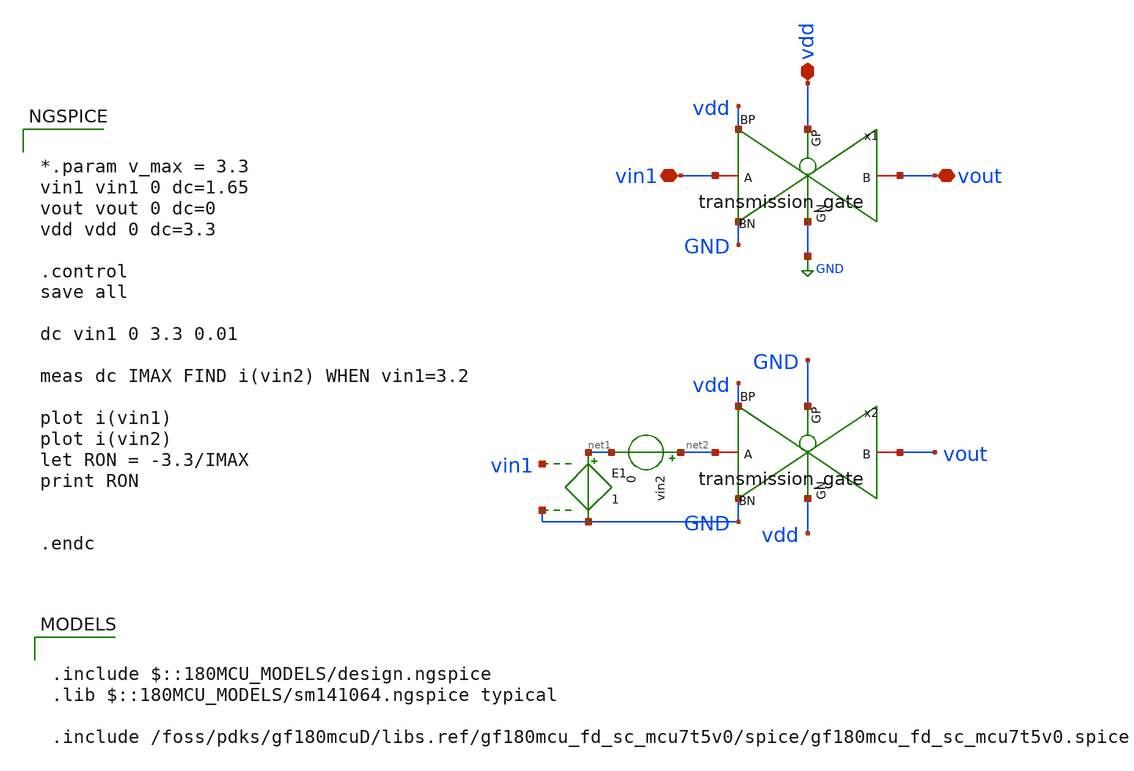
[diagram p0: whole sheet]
** sch_path: designs/switch_matrix_gf180mcu_9t5v0-main/tgate_PK_5V/old/tb_transmission_gate.sch
**.subckt tb_transmission_gate vin1 vout vdd
*.iopin vin1
*.iopin vout
*.iopin vdd
x1 vout GND vdd vin1 vdd GND transmission_gate
x2 vout vdd GND net2 vdd GND transmission_gate
E1 net1 GND vin1 GND 1
vin2 net2 net1 0
**** begin user architecture code


*.param v_max = 3.3
vin1 vin1 0 dc=1.65
vout vout 0 dc=0
vdd vdd 0 dc=3.3

.control
save all

dc vin1 0 3.3 0.01

meas dc IMAX FIND i(vin2) WHEN vin1=3.2

plot i(vin1)
plot i(vin2)
let RON = -3.3/IMAX
print RON


.endc



.include $::180MCU_MODELS/design.ngspice
.lib $::180MCU_MODELS/sm141064.ngspice typical

.include /foss/pdks/gf180mcuD/libs.ref/gf180mcu_fd_sc_mcu7t5v0/spice/gf180mcu_fd_sc_mcu7t5v0.spice

**** end user architecture code
**.ends

* expanding   symbol:  transmission_gate.sym # of pins=6
** sym_path: designs/switch_matrix_gf180mcu_9t5v0-main/tgate_PK/transmission_gate.sym
** sch_path: designs/switch_matrix_gf180mcu_9t5v0-main/tgate_PK/transmission_gate.sch
.subckt transmission_gate B GN GP A BP BN
*.iopin B
*.iopin GN
*.iopin A
*.iopin GP
*.iopin BN
*.iopin BP
XM1 A GN B BN nfet_03v3 L=0.28u W=mn_w nf=6 ad='int((nf+1)/2) * W/nf * 0.18u' as='int((nf+2)/2) * W/nf * 0.18u'
+ pd='2*int((nf+1)/2) * (W/nf + 0.18u)' ps='2*int((nf+2)/2) * (W/nf + 0.18u)' nrd='0.18u / W' nrs='0.18u / W'
+ sa=0 sb=0 sd=0 m=1
XM2 A GP B BP pfet_03v3 L=0.28u W=mp_w nf=6 ad='int((nf+1)/2) * W/nf * 0.18u' as='int((nf+2)/2) * W/nf * 0.18u'
+ pd='2*int((nf+1)/2) * (W/nf + 0.18u)' ps='2*int((nf+2)/2) * (W/nf + 0.18u)' nrd='0.18u / W' nrs='0.18u / W'
+ sa=0 sb=0 sd=0 m=1
.ends

.GLOBAL GND
.end
